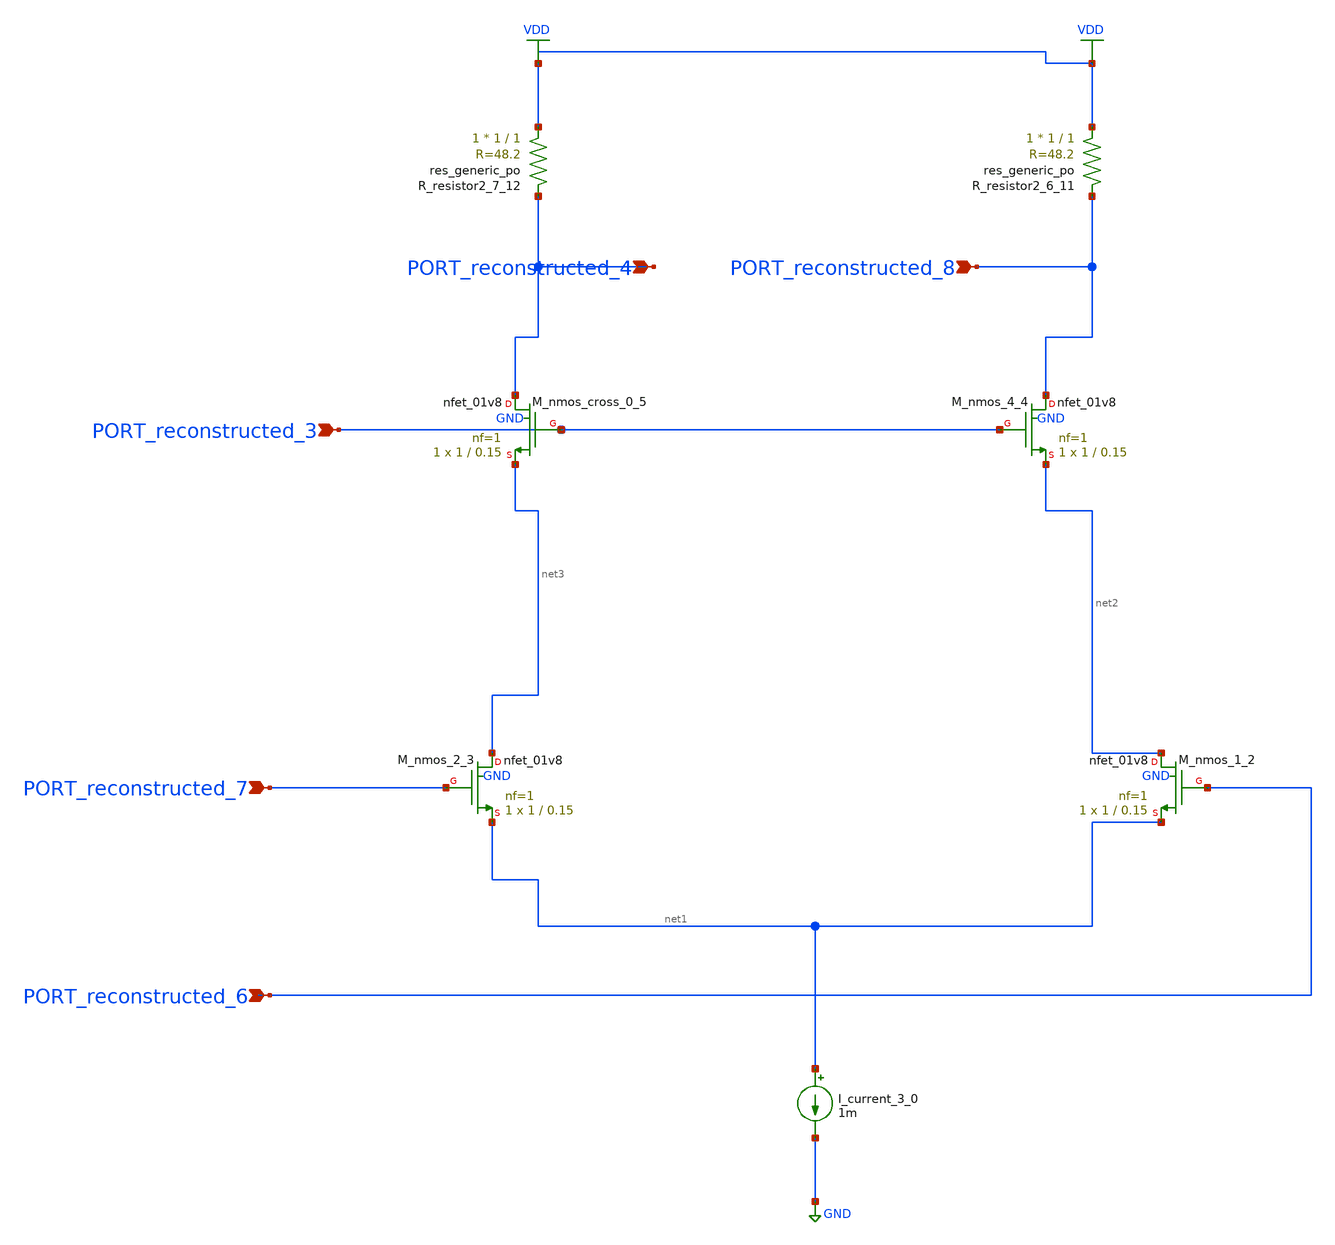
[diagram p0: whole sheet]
** sch_path: schematics/AMSNet/817.sch
**.subckt 817 PORT_reconstructed_6 PORT_reconstructed_3 PORT_reconstructed_7 PORT_reconstructed_4
*+ PORT_reconstructed_8
*.ipin PORT_reconstructed_6
*.ipin PORT_reconstructed_3
*.ipin PORT_reconstructed_7
*.ipin PORT_reconstructed_4
*.ipin PORT_reconstructed_8
I_current_3_0 net1 GND 1m
XM_nmos_1_2 net2 PORT_reconstructed_6 net1 GND sky130_fd_pr__nfet_01v8 L=0.15 W=1 nf=1 ad='int((1 + 1)/2) * 1 / 1 * 0.29'
+ as='int((1 + 2)/2) * 1 / 1 * 0.29' pd='2*int((1 + 1)/2) * (1 / 1 + 0.29)' ps='2*int((1 + 2)/2) * (1 / 1 + 0.29)'
+ nrd='0.29 / 1 ' nrs='0.29 / 1 ' sa=0 sb=0 sd=0 mult=1 m=1
XM_nmos_2_3 net3 PORT_reconstructed_7 net1 GND sky130_fd_pr__nfet_01v8 L=0.15 W=1 nf=1 ad='int((1 + 1)/2) * 1 / 1 * 0.29'
+ as='int((1 + 2)/2) * 1 / 1 * 0.29' pd='2*int((1 + 1)/2) * (1 / 1 + 0.29)' ps='2*int((1 + 2)/2) * (1 / 1 + 0.29)'
+ nrd='0.29 / 1 ' nrs='0.29 / 1 ' sa=0 sb=0 sd=0 mult=1 m=1
XM_nmos_4_4 PORT_reconstructed_8 PORT_reconstructed_3 net2 GND sky130_fd_pr__nfet_01v8 L=0.15 W=1 nf=1
+ ad='int((1 + 1)/2) * 1 / 1 * 0.29' as='int((1 + 2)/2) * 1 / 1 * 0.29' pd='2*int((1 + 1)/2) * (1 / 1 + 0.29)'
+ ps='2*int((1 + 2)/2) * (1 / 1 + 0.29)' nrd='0.29 / 1 ' nrs='0.29 / 1 ' sa=0 sb=0 sd=0 mult=1 m=1
XM_nmos_cross_0_5 PORT_reconstructed_4 PORT_reconstructed_3 net3 GND sky130_fd_pr__nfet_01v8 L=0.15 W=1
+ nf=1 ad='int((1 + 1)/2) * 1 / 1 * 0.29' as='int((1 + 2)/2) * 1 / 1 * 0.29' pd='2*int((1 + 1)/2) * (1 / 1 + 0.29)'
+ ps='2*int((1 + 2)/2) * (1 / 1 + 0.29)' nrd='0.29 / 1 ' nrs='0.29 / 1 ' sa=0 sb=0 sd=0 mult=1 m=1
XR_resistor2_6_11 VDD PORT_reconstructed_8 sky130_fd_pr__res_generic_po W=1 L=1 m=1
XR_resistor2_7_12 VDD PORT_reconstructed_4 sky130_fd_pr__res_generic_po W=1 L=1 m=1
**.ends
.GLOBAL GND
.GLOBAL VDD
.end
